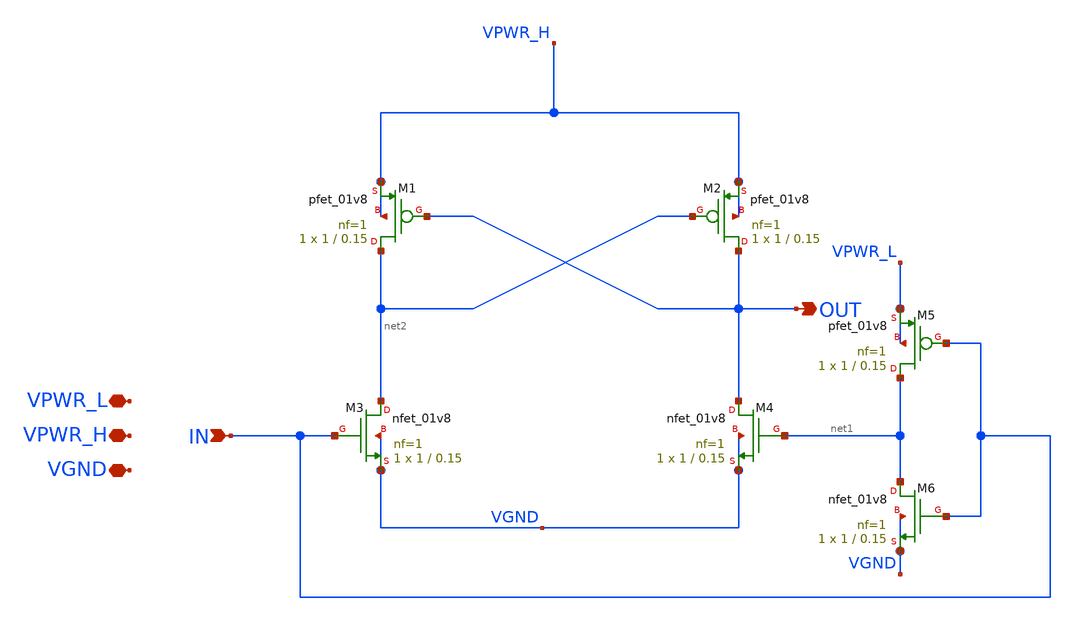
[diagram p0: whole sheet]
** sch_path: xschem/level_shifter.sch
**.subckt level_shifter VGND VPWR_H VPWR_L IN OUT
*.iopin VGND
*.iopin VPWR_H
*.iopin VPWR_L
*.ipin IN
*.opin OUT
XM1 net2 OUT VPWR_H VPWR_H sky130_fd_pr__pfet_01v8 L=0.15 W=1 nf=1 ad='int((nf+1)/2) * W/nf * 0.29' as='int((nf+2)/2) * W/nf * 0.29'
+ pd='2*int((nf+1)/2) * (W/nf + 0.29)' ps='2*int((nf+2)/2) * (W/nf + 0.29)' nrd='0.29 / W' nrs='0.29 / W'
+ sa=0 sb=0 sd=0 mult=1 m=1
XM2 OUT net2 VPWR_H VPWR_H sky130_fd_pr__pfet_01v8 L=0.15 W=1 nf=1 ad='int((nf+1)/2) * W/nf * 0.29' as='int((nf+2)/2) * W/nf * 0.29'
+ pd='2*int((nf+1)/2) * (W/nf + 0.29)' ps='2*int((nf+2)/2) * (W/nf + 0.29)' nrd='0.29 / W' nrs='0.29 / W'
+ sa=0 sb=0 sd=0 mult=1 m=1
XM3 net2 IN VGND VGND sky130_fd_pr__nfet_01v8 L=0.15 W=1 nf=1 ad='int((nf+1)/2) * W/nf * 0.29' as='int((nf+2)/2) * W/nf * 0.29'
+ pd='2*int((nf+1)/2) * (W/nf + 0.29)' ps='2*int((nf+2)/2) * (W/nf + 0.29)' nrd='0.29 / W' nrs='0.29 / W'
+ sa=0 sb=0 sd=0 mult=1 m=1
XM4 OUT net1 VGND VGND sky130_fd_pr__nfet_01v8 L=0.15 W=1 nf=1 ad='int((nf+1)/2) * W/nf * 0.29' as='int((nf+2)/2) * W/nf * 0.29'
+ pd='2*int((nf+1)/2) * (W/nf + 0.29)' ps='2*int((nf+2)/2) * (W/nf + 0.29)' nrd='0.29 / W' nrs='0.29 / W'
+ sa=0 sb=0 sd=0 mult=1 m=1
XM5 net1 IN VPWR_L VPWR_L sky130_fd_pr__pfet_01v8 L=0.15 W=1 nf=1 ad='int((nf+1)/2) * W/nf * 0.29' as='int((nf+2)/2) * W/nf * 0.29'
+ pd='2*int((nf+1)/2) * (W/nf + 0.29)' ps='2*int((nf+2)/2) * (W/nf + 0.29)' nrd='0.29 / W' nrs='0.29 / W'
+ sa=0 sb=0 sd=0 mult=1 m=1
XM6 net1 IN VGND VGND sky130_fd_pr__nfet_01v8 L=0.15 W=1 nf=1 ad='int((nf+1)/2) * W/nf * 0.29' as='int((nf+2)/2) * W/nf * 0.29'
+ pd='2*int((nf+1)/2) * (W/nf + 0.29)' ps='2*int((nf+2)/2) * (W/nf + 0.29)' nrd='0.29 / W' nrs='0.29 / W'
+ sa=0 sb=0 sd=0 mult=1 m=1
**.ends
.end
